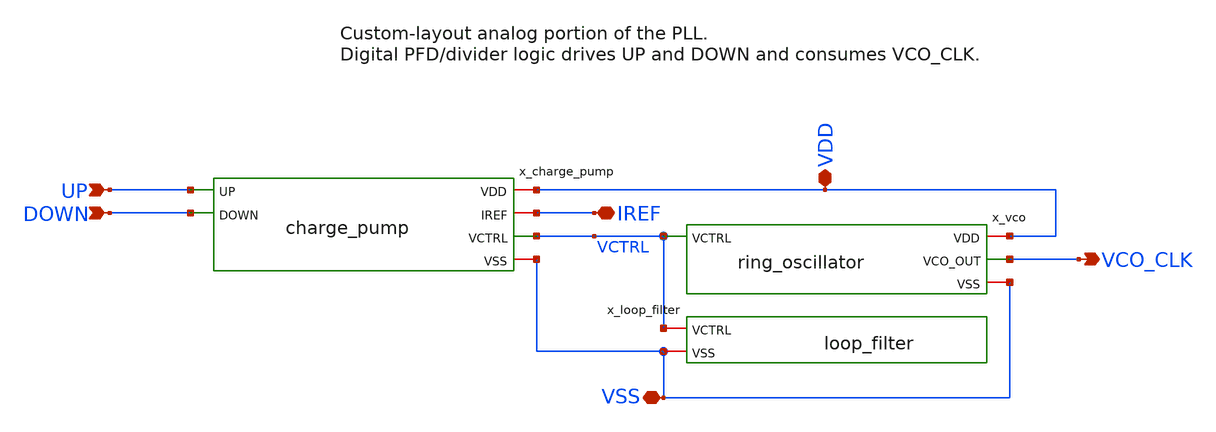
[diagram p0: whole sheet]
** sch_path: macros/pll_analog/schematic/xschem/pll_analog.sch
**.subckt pll_analog UP DOWN IREF VCO_CLK VDD VSS
*.ipin UP
*.ipin DOWN
*.iopin IREF
*.opin VCO_CLK
*.iopin VDD
*.iopin VSS
x_charge_pump VDD UP DOWN IREF VCTRL VSS charge_pump
x_loop_filter VCTRL VSS loop_filter
x_vco VDD VCO_CLK VCTRL VSS ring_oscillator
**.ends
.end
